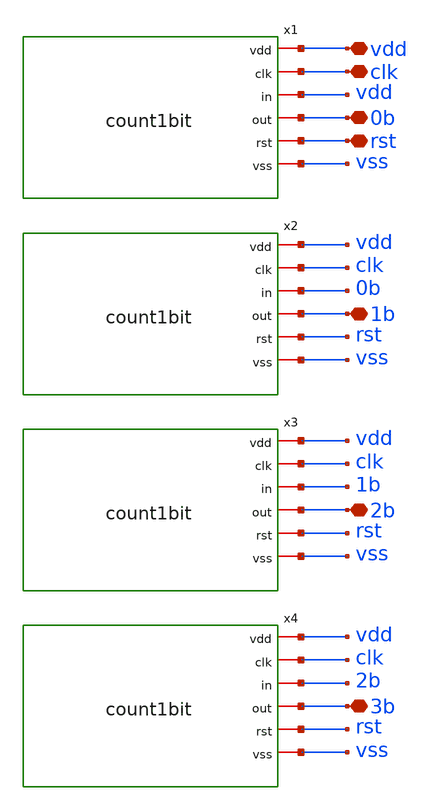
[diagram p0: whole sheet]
** sch_path: design/blocks/count4bits/schematic/count4bits.sch
**.subckt count4bits vdd clk rst 0b 1b 2b 3b
*.iopin vdd
*.iopin clk
*.iopin rst
*.iopin 0b
*.iopin 1b
*.iopin 2b
*.iopin 3b
x1 vdd clk vdd 0b rst vss count1bit
x2 vdd clk 0b 1b rst vss count1bit
x3 vdd clk 1b 2b rst vss count1bit
x4 vdd clk 2b 3b rst vss count1bit
**.ends
.end
